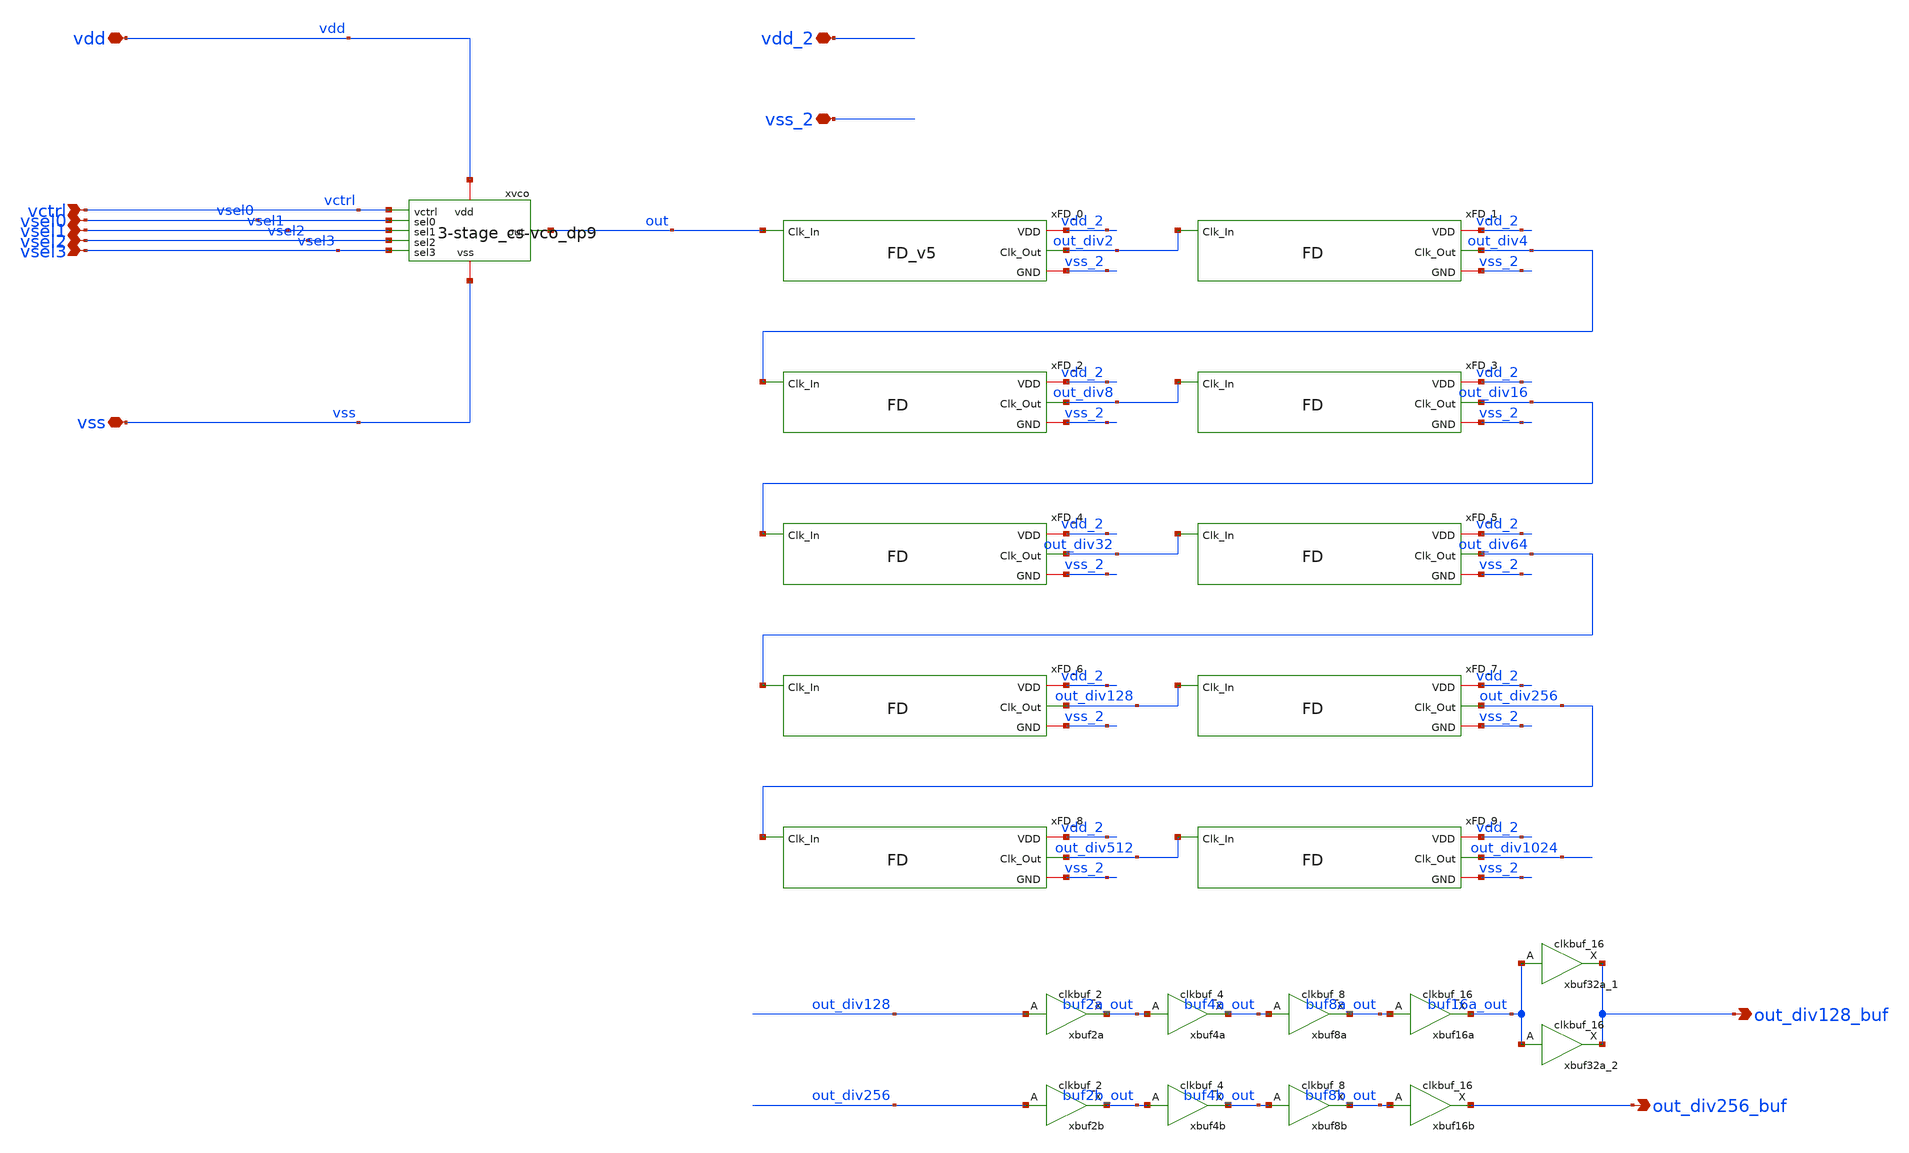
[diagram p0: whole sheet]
** sch_path: xschem/3-stage_cs-vco_dp9/vco_with_fdivs_split_supplies.sch
**.subckt vco_with_fdivs_split_supplies vctrl out_div128_buf vdd vss vsel0 vsel1 vsel2 vsel3
*+ out_div256_buf vdd_2 vss_2
*.ipin vctrl
*.opin out_div128_buf
*.iopin vdd
*.iopin vss
*.ipin vsel0
*.ipin vsel1
*.ipin vsel2
*.ipin vsel3
*.opin out_div256_buf
*.iopin vdd_2
*.iopin vss_2
xvco vdd out vctrl vss vsel0 vsel1 vsel2 vsel3 3-stage_cs-vco_dp9
xFD_0 vdd_2 out_div2 vss_2 out FD_v5
xbuf2a out_div128 vss_2 vss_2 vdd_2 vdd_2 buf2a_out sky130_fd_sc_hd__clkbuf_2
xbuf4a buf2a_out vss_2 vss_2 vdd_2 vdd_2 buf4a_out sky130_fd_sc_hd__clkbuf_4
xbuf8a buf4a_out vss_2 vss_2 vdd_2 vdd_2 buf8a_out sky130_fd_sc_hd__clkbuf_8
xFD_1 vdd_2 out_div4 vss_2 out_div2 FD
xFD_2 vdd_2 out_div8 vss_2 out_div4 FD
xFD_3 vdd_2 out_div16 vss_2 out_div8 FD
xFD_4 vdd_2 out_div32 vss_2 out_div16 FD
xFD_5 vdd_2 out_div64 vss_2 out_div32 FD
xFD_6 vdd_2 out_div128 vss_2 out_div64 FD
xFD_7 vdd_2 out_div256 vss_2 out_div128 FD
xbuf2b out_div256 vss_2 vss_2 vdd_2 vdd_2 buf2b_out sky130_fd_sc_hd__clkbuf_2
xbuf4b buf2b_out vss_2 vss_2 vdd_2 vdd_2 buf4b_out sky130_fd_sc_hd__clkbuf_4
xbuf8b buf4b_out vss_2 vss_2 vdd_2 vdd buf8b_out sky130_fd_sc_hd__clkbuf_8
xFD_8 vdd_2 out_div512 vss_2 out_div256 FD
xFD_9 vdd_2 out_div1024 vss_2 out_div512 FD
xbuf16a buf8a_out vss_2 vss_2 vdd_2 vdd_2 buf16a_out sky130_fd_sc_hd__clkbuf_16
xbuf16b buf8b_out vss_2 vss_2 vdd_2 vdd_2 out_div256_buf sky130_fd_sc_hd__clkbuf_16
xbuf32a_1 buf16a_out vss_2 vss_2 vdd_2 vdd_2 out_div128_buf sky130_fd_sc_hd__clkbuf_16
xbuf32a_2 buf16a_out vss_2 vss_2 vdd_2 vdd_2 out_div128_buf sky130_fd_sc_hd__clkbuf_16
**.ends

* expanding   symbol:  3-stage_cs-vco_dp9.sym # of pins=8
** sym_path: xschem/3-stage_cs-vco_dp9/3-stage_cs-vco_dp9.sym
** sch_path: xschem/3-stage_cs-vco_dp9/3-stage_cs-vco_dp9.sch
.subckt 3-stage_cs-vco_dp9 vdd out vctrl vss sel0 sel1 sel2 sel3
*.iopin vdd
*.iopin vss
*.opin out
*.ipin vctrl
*.ipin sel0
*.ipin sel1
*.ipin sel2
*.ipin sel3
XM25 vgp vgp vdd vdd sky130_fd_pr__pfet_01v8 L=0.18 W=1 nf=1 ad='int((nf+1)/2) * W/nf * 0.29' as='int((nf+2)/2) * W/nf * 0.29'
+ pd='2*int((nf+1)/2) * (W/nf + 0.29)' ps='2*int((nf+2)/2) * (W/nf + 0.29)' nrd='0.29 / W' nrs='0.29 / W'
+ sa=0 sb=0 sd=0 mult=1 m=1
XM26 vgp vctrl vss vss sky130_fd_pr__nfet_01v8 L=0.18 W=1 nf=1 ad='int((nf+1)/2) * W/nf * 0.29' as='int((nf+2)/2) * W/nf * 0.29'
+ pd='2*int((nf+1)/2) * (W/nf + 0.29)' ps='2*int((nf+2)/2) * (W/nf + 0.29)' nrd='0.29 / W' nrs='0.29 / W'
+ sa=0 sb=0 sd=0 mult=1 m=1
XM11C net2 pg2 vdd vdd sky130_fd_pr__pfet_01v8 L=0.18 W=2.4 nf=1 ad='int((nf+1)/2) * W/nf * 0.29' as='int((nf+2)/2) * W/nf * 0.29'
+ pd='2*int((nf+1)/2) * (W/nf + 0.29)' ps='2*int((nf+2)/2) * (W/nf + 0.29)' nrd='0.29 / W' nrs='0.29 / W'
+ sa=0 sb=0 sd=0 mult=1 m=1
XM16A net8 ng0 vss vss sky130_fd_pr__nfet_01v8 L=0.18 W=0.6 nf=1 ad='int((nf+1)/2) * W/nf * 0.29' as='int((nf+2)/2) * W/nf * 0.29'
+ pd='2*int((nf+1)/2) * (W/nf + 0.29)' ps='2*int((nf+2)/2) * (W/nf + 0.29)' nrd='0.29 / W' nrs='0.29 / W'
+ sa=0 sb=0 sd=0 mult=1 m=1
XM1 net3 net5 net2 vdd sky130_fd_pr__pfet_01v8 L=0.15 W=1.4 nf=1 ad='int((nf+1)/2) * W/nf * 0.29' as='int((nf+2)/2) * W/nf * 0.29'
+ pd='2*int((nf+1)/2) * (W/nf + 0.29)' ps='2*int((nf+2)/2) * (W/nf + 0.29)' nrd='0.29 / W' nrs='0.29 / W'
+ sa=0 sb=0 sd=0 mult=1 m=1
XM3 net4 net3 vdd vdd sky130_fd_pr__pfet_01v8 L=0.15 W=0.75 nf=1 ad='int((nf+1)/2) * W/nf * 0.29' as='int((nf+2)/2) * W/nf * 0.29'
+ pd='2*int((nf+1)/2) * (W/nf + 0.29)' ps='2*int((nf+2)/2) * (W/nf + 0.29)' nrd='0.29 / W' nrs='0.29 / W'
+ sa=0 sb=0 sd=0 mult=1 m=1
XM5 net5 net4 vdd vdd sky130_fd_pr__pfet_01v8 L=0.15 W=3 nf=1 ad='int((nf+1)/2) * W/nf * 0.29' as='int((nf+2)/2) * W/nf * 0.29'
+ pd='2*int((nf+1)/2) * (W/nf + 0.29)' ps='2*int((nf+2)/2) * (W/nf + 0.29)' nrd='0.29 / W' nrs='0.29 / W'
+ sa=0 sb=0 sd=0 mult=1 m=1
XM2 net3 net5 net8 vss sky130_fd_pr__nfet_01v8 L=0.15 W=0.72 nf=1 ad='int((nf+1)/2) * W/nf * 0.29' as='int((nf+2)/2) * W/nf * 0.29'
+ pd='2*int((nf+1)/2) * (W/nf + 0.29)' ps='2*int((nf+2)/2) * (W/nf + 0.29)' nrd='0.29 / W' nrs='0.29 / W'
+ sa=0 sb=0 sd=0 mult=1 m=1
XM4 net4 net3 vss vss sky130_fd_pr__nfet_01v8 L=0.15 W=0.5 nf=1 ad='int((nf+1)/2) * W/nf * 0.29' as='int((nf+2)/2) * W/nf * 0.29'
+ pd='2*int((nf+1)/2) * (W/nf + 0.29)' ps='2*int((nf+2)/2) * (W/nf + 0.29)' nrd='0.29 / W' nrs='0.29 / W'
+ sa=0 sb=0 sd=0 mult=1 m=1
XM6 net5 net4 vss vss sky130_fd_pr__nfet_01v8 L=0.15 W=1.44 nf=1 ad='int((nf+1)/2) * W/nf * 0.29' as='int((nf+2)/2) * W/nf * 0.29'
+ pd='2*int((nf+1)/2) * (W/nf + 0.29)' ps='2*int((nf+2)/2) * (W/nf + 0.29)' nrd='0.29 / W' nrs='0.29 / W'
+ sa=0 sb=0 sd=0 mult=1 m=1
XM21 net6 net5 vdd vdd sky130_fd_pr__pfet_01v8 L=0.15 W=0.8 nf=1 ad='int((nf+1)/2) * W/nf * 0.29' as='int((nf+2)/2) * W/nf * 0.29'
+ pd='2*int((nf+1)/2) * (W/nf + 0.29)' ps='2*int((nf+2)/2) * (W/nf + 0.29)' nrd='0.29 / W' nrs='0.29 / W'
+ sa=0 sb=0 sd=0 mult=1 m=1
XM22 net6 net5 vss vss sky130_fd_pr__nfet_01v8 L=0.15 W=0.42 nf=1 ad='int((nf+1)/2) * W/nf * 0.29' as='int((nf+2)/2) * W/nf * 0.29'
+ pd='2*int((nf+1)/2) * (W/nf + 0.29)' ps='2*int((nf+2)/2) * (W/nf + 0.29)' nrd='0.29 / W' nrs='0.29 / W'
+ sa=0 sb=0 sd=0 mult=1 m=1
XM23 out net7 vdd vdd sky130_fd_pr__pfet_01v8 L=0.18 W=6.6 nf=3 ad='int((nf+1)/2) * W/nf * 0.29' as='int((nf+2)/2) * W/nf * 0.29'
+ pd='2*int((nf+1)/2) * (W/nf + 0.29)' ps='2*int((nf+2)/2) * (W/nf + 0.29)' nrd='0.29 / W' nrs='0.29 / W'
+ sa=0 sb=0 sd=0 mult=1 m=1
XM24 out net7 vss vss sky130_fd_pr__nfet_01v8 L=0.18 W=1.29 nf=1 ad='int((nf+1)/2) * W/nf * 0.29' as='int((nf+2)/2) * W/nf * 0.29'
+ pd='2*int((nf+1)/2) * (W/nf + 0.29)' ps='2*int((nf+2)/2) * (W/nf + 0.29)' nrd='0.29 / W' nrs='0.29 / W'
+ sa=0 sb=0 sd=0 mult=1 m=1
XM12 net7 net6 vdd vdd sky130_fd_pr__pfet_01v8 L=0.15 W=2.4 nf=1 ad='int((nf+1)/2) * W/nf * 0.29' as='int((nf+2)/2) * W/nf * 0.29'
+ pd='2*int((nf+1)/2) * (W/nf + 0.29)' ps='2*int((nf+2)/2) * (W/nf + 0.29)' nrd='0.29 / W' nrs='0.29 / W'
+ sa=0 sb=0 sd=0 mult=1 m=1
XM13 net7 net6 vss vss sky130_fd_pr__nfet_01v8 L=0.15 W=1.2 nf=1 ad='int((nf+1)/2) * W/nf * 0.29' as='int((nf+2)/2) * W/nf * 0.29'
+ pd='2*int((nf+1)/2) * (W/nf + 0.29)' ps='2*int((nf+2)/2) * (W/nf + 0.29)' nrd='0.29 / W' nrs='0.29 / W'
+ sa=0 sb=0 sd=0 mult=1 m=1
XMDUM16B vss vss vss vss sky130_fd_pr__nfet_01v8 L=0.18 W=2.4 nf=1 ad='int((nf+1)/2) * W/nf * 0.29' as='int((nf+2)/2) * W/nf * 0.29'
+ pd='2*int((nf+1)/2) * (W/nf + 0.29)' ps='2*int((nf+2)/2) * (W/nf + 0.29)' nrd='0.29 / W' nrs='0.29 / W'
+ sa=0 sb=0 sd=0 mult=1 m=1
XMDUM16 vss vss vss vss sky130_fd_pr__nfet_01v8 L=0.18 W=2.4 nf=1 ad='int((nf+1)/2) * W/nf * 0.29' as='int((nf+2)/2) * W/nf * 0.29'
+ pd='2*int((nf+1)/2) * (W/nf + 0.29)' ps='2*int((nf+2)/2) * (W/nf + 0.29)' nrd='0.29 / W' nrs='0.29 / W'
+ sa=0 sb=0 sd=0 mult=1 m=1
XMDUM26 vss vss vss vss sky130_fd_pr__nfet_01v8 L=0.18 W=1 nf=1 ad='int((nf+1)/2) * W/nf * 0.29' as='int((nf+2)/2) * W/nf * 0.29'
+ pd='2*int((nf+1)/2) * (W/nf + 0.29)' ps='2*int((nf+2)/2) * (W/nf + 0.29)' nrd='0.29 / W' nrs='0.29 / W'
+ sa=0 sb=0 sd=0 mult=1 m=1
XMDUM11B vdd vdd vdd vdd sky130_fd_pr__pfet_01v8 L=0.18 W=2.4 nf=1 ad='int((nf+1)/2) * W/nf * 0.29' as='int((nf+2)/2) * W/nf * 0.29'
+ pd='2*int((nf+1)/2) * (W/nf + 0.29)' ps='2*int((nf+2)/2) * (W/nf + 0.29)' nrd='0.29 / W' nrs='0.29 / W'
+ sa=0 sb=0 sd=0 mult=1 m=1
XMDUM11 vdd vdd vdd vdd sky130_fd_pr__pfet_01v8 L=0.18 W=2.4 nf=1 ad='int((nf+1)/2) * W/nf * 0.29' as='int((nf+2)/2) * W/nf * 0.29'
+ pd='2*int((nf+1)/2) * (W/nf + 0.29)' ps='2*int((nf+2)/2) * (W/nf + 0.29)' nrd='0.29 / W' nrs='0.29 / W'
+ sa=0 sb=0 sd=0 mult=1 m=1
XMDUM25 vdd vdd vdd vdd sky130_fd_pr__pfet_01v8 L=0.18 W=1 nf=1 ad='int((nf+1)/2) * W/nf * 0.29' as='int((nf+2)/2) * W/nf * 0.29'
+ pd='2*int((nf+1)/2) * (W/nf + 0.29)' ps='2*int((nf+2)/2) * (W/nf + 0.29)' nrd='0.29 / W' nrs='0.29 / W'
+ sa=0 sb=0 sd=0 mult=1 m=1
Cnet8 net3 vss 0.87f m=1
Cnet9 net4 vss 1.14f m=1
Cnet10 net5 vss 3.49f m=1
XMDUM26B vss vss vss vss sky130_fd_pr__nfet_01v8 L=0.18 W=1 nf=1 ad='int((nf+1)/2) * W/nf * 0.29' as='int((nf+2)/2) * W/nf * 0.29'
+ pd='2*int((nf+1)/2) * (W/nf + 0.29)' ps='2*int((nf+2)/2) * (W/nf + 0.29)' nrd='0.29 / W' nrs='0.29 / W'
+ sa=0 sb=0 sd=0 mult=1 m=1
XMDUM25B vdd vdd vdd vdd sky130_fd_pr__pfet_01v8 L=0.18 W=1 nf=1 ad='int((nf+1)/2) * W/nf * 0.29' as='int((nf+2)/2) * W/nf * 0.29'
+ pd='2*int((nf+1)/2) * (W/nf + 0.29)' ps='2*int((nf+2)/2) * (W/nf + 0.29)' nrd='0.29 / W' nrs='0.29 / W'
+ sa=0 sb=0 sd=0 mult=1 m=1
x1n vdd ng0 vctrl vss sel0 vco_switch_n
XM16B net8 ng1 vss vss sky130_fd_pr__nfet_01v8 L=0.18 W=1.2 nf=1 ad='int((nf+1)/2) * W/nf * 0.29' as='int((nf+2)/2) * W/nf * 0.29'
+ pd='2*int((nf+1)/2) * (W/nf + 0.29)' ps='2*int((nf+2)/2) * (W/nf + 0.29)' nrd='0.29 / W' nrs='0.29 / W'
+ sa=0 sb=0 sd=0 mult=1 m=1
x2n vdd ng1 vctrl vss sel1 vco_switch_n
XM16C net8 ng2 vss vss sky130_fd_pr__nfet_01v8 L=0.18 W=2.4 nf=1 ad='int((nf+1)/2) * W/nf * 0.29' as='int((nf+2)/2) * W/nf * 0.29'
+ pd='2*int((nf+1)/2) * (W/nf + 0.29)' ps='2*int((nf+2)/2) * (W/nf + 0.29)' nrd='0.29 / W' nrs='0.29 / W'
+ sa=0 sb=0 sd=0 mult=1 m=1
x3n vdd ng2 vctrl vss sel2 vco_switch_n
XM16D net8 ng3 vss vss sky130_fd_pr__nfet_01v8 L=0.18 W=2.4 nf=1 ad='int((nf+1)/2) * W/nf * 0.29' as='int((nf+2)/2) * W/nf * 0.29'
+ pd='2*int((nf+1)/2) * (W/nf + 0.29)' ps='2*int((nf+2)/2) * (W/nf + 0.29)' nrd='0.29 / W' nrs='0.29 / W'
+ sa=0 sb=0 sd=0 mult=2 m=2
x4n vdd ng3 vctrl vss sel3 vco_switch_n
x3p vdd pg2 vgp vss sel2 vco_switch_p
XM11D net2 pg3 vdd vdd sky130_fd_pr__pfet_01v8 L=0.18 W=2.4 nf=1 ad='int((nf+1)/2) * W/nf * 0.29' as='int((nf+2)/2) * W/nf * 0.29'
+ pd='2*int((nf+1)/2) * (W/nf + 0.29)' ps='2*int((nf+2)/2) * (W/nf + 0.29)' nrd='0.29 / W' nrs='0.29 / W'
+ sa=0 sb=0 sd=0 mult=2 m=2
x4p vdd pg3 vgp vss sel3 vco_switch_p
XM11B net2 pg1 vdd vdd sky130_fd_pr__pfet_01v8 L=0.18 W=1.2 nf=1 ad='int((nf+1)/2) * W/nf * 0.29' as='int((nf+2)/2) * W/nf * 0.29'
+ pd='2*int((nf+1)/2) * (W/nf + 0.29)' ps='2*int((nf+2)/2) * (W/nf + 0.29)' nrd='0.29 / W' nrs='0.29 / W'
+ sa=0 sb=0 sd=0 mult=1 m=1
x2p vdd pg1 vgp vss sel1 vco_switch_p
XM11A net2 pg0 vdd vdd sky130_fd_pr__pfet_01v8 L=0.18 W=0.6 nf=1 ad='int((nf+1)/2) * W/nf * 0.29' as='int((nf+2)/2) * W/nf * 0.29'
+ pd='2*int((nf+1)/2) * (W/nf + 0.29)' ps='2*int((nf+2)/2) * (W/nf + 0.29)' nrd='0.29 / W' nrs='0.29 / W'
+ sa=0 sb=0 sd=0 mult=1 m=1
x1p vdd pg0 vgp vss sel0 vco_switch_p
XM16 net8 vctrl vss vss sky130_fd_pr__nfet_01v8 L=0.18 W=0.6 nf=1 ad='int((nf+1)/2) * W/nf * 0.29' as='int((nf+2)/2) * W/nf * 0.29'
+ pd='2*int((nf+1)/2) * (W/nf + 0.29)' ps='2*int((nf+2)/2) * (W/nf + 0.29)' nrd='0.29 / W' nrs='0.29 / W'
+ sa=0 sb=0 sd=0 mult=1 m=1
XM11 net2 vgp vdd vdd sky130_fd_pr__pfet_01v8 L=0.18 W=0.6 nf=1 ad='int((nf+1)/2) * W/nf * 0.29' as='int((nf+2)/2) * W/nf * 0.29'
+ pd='2*int((nf+1)/2) * (W/nf + 0.29)' ps='2*int((nf+2)/2) * (W/nf + 0.29)' nrd='0.29 / W' nrs='0.29 / W'
+ sa=0 sb=0 sd=0 mult=1 m=1
.ends


* expanding   symbol:  FD_v5.sym # of pins=4
** sym_path: xschem/3-stage_cs-vco_dp9/FD_v5.sym
** sch_path: xschem/3-stage_cs-vco_dp9/FD_v5.sch
.subckt FD_v5 VDD Clk_Out GND Clk_In
*.ipin Clk_In
*.iopin VDD
*.iopin GND
*.opin Clk_Out
XMPbuf1 7 6 VDD VDD sky130_fd_pr__pfet_01v8 L=0.15 W=1.44 nf=1 ad='int((nf+1)/2) * W/nf * 0.29' as='int((nf+2)/2) * W/nf * 0.29'
+ pd='2*int((nf+1)/2) * (W/nf + 0.29)' ps='2*int((nf+2)/2) * (W/nf + 0.29)' nrd='0.29 / W' nrs='0.29 / W'
+ sa=0 sb=0 sd=0 mult=1 m=1
XMNbuf1 7 6 GND GND sky130_fd_pr__nfet_01v8 L=0.15 W=0.84 nf=1 ad='int((nf+1)/2) * W/nf * 0.29' as='int((nf+2)/2) * W/nf * 0.29'
+ pd='2*int((nf+1)/2) * (W/nf + 0.29)' ps='2*int((nf+2)/2) * (W/nf + 0.29)' nrd='0.29 / W' nrs='0.29 / W'
+ sa=0 sb=0 sd=0 mult=1 m=1
XMPClkin Clk_In_buf Clkb_buf VDD VDD sky130_fd_pr__pfet_01v8 L=0.15 W=1.44 nf=1 ad='int((nf+1)/2) * W/nf * 0.29'
+ as='int((nf+2)/2) * W/nf * 0.29' pd='2*int((nf+1)/2) * (W/nf + 0.29)' ps='2*int((nf+2)/2) * (W/nf + 0.29)'
+ nrd='0.29 / W' nrs='0.29 / W' sa=0 sb=0 sd=0 mult=4 m=4
XMNClkin Clk_In_buf Clkb_buf GND GND sky130_fd_pr__nfet_01v8 L=0.15 W=0.84 nf=1 ad='int((nf+1)/2) * W/nf * 0.29'
+ as='int((nf+2)/2) * W/nf * 0.29' pd='2*int((nf+1)/2) * (W/nf + 0.29)' ps='2*int((nf+2)/2) * (W/nf + 0.29)'
+ nrd='0.29 / W' nrs='0.29 / W' sa=0 sb=0 sd=0 mult=3 m=3
XMPinv2 5 4 VDD VDD sky130_fd_pr__pfet_01v8 L=0.15 W=1.44 nf=1 ad='int((nf+1)/2) * W/nf * 0.29' as='int((nf+2)/2) * W/nf * 0.29'
+ pd='2*int((nf+1)/2) * (W/nf + 0.29)' ps='2*int((nf+2)/2) * (W/nf + 0.29)' nrd='0.29 / W' nrs='0.29 / W'
+ sa=0 sb=0 sd=0 mult=4 m=4
XMNinv2 5 4 GND GND sky130_fd_pr__nfet_01v8 L=0.15 W=0.84 nf=1 ad='int((nf+1)/2) * W/nf * 0.29' as='int((nf+2)/2) * W/nf * 0.29'
+ pd='2*int((nf+1)/2) * (W/nf + 0.29)' ps='2*int((nf+2)/2) * (W/nf + 0.29)' nrd='0.29 / W' nrs='0.29 / W'
+ sa=0 sb=0 sd=0 mult=3 m=3
XMPinv1 3 2 VDD VDD sky130_fd_pr__pfet_01v8 L=0.15 W=1.44 nf=1 ad='int((nf+1)/2) * W/nf * 0.29' as='int((nf+2)/2) * W/nf * 0.29'
+ pd='2*int((nf+1)/2) * (W/nf + 0.29)' ps='2*int((nf+2)/2) * (W/nf + 0.29)' nrd='0.29 / W' nrs='0.29 / W'
+ sa=0 sb=0 sd=0 mult=4 m=4
XMNinv1 3 2 GND GND sky130_fd_pr__nfet_01v8 L=0.15 W=0.84 nf=1 ad='int((nf+1)/2) * W/nf * 0.29' as='int((nf+2)/2) * W/nf * 0.29'
+ pd='2*int((nf+1)/2) * (W/nf + 0.29)' ps='2*int((nf+2)/2) * (W/nf + 0.29)' nrd='0.29 / W' nrs='0.29 / W'
+ sa=0 sb=0 sd=0 mult=3 m=3
XMPTgate1 4 Clkb_buf 3 VDD sky130_fd_pr__pfet_01v8 L=0.15 W=1.44 nf=1 ad='int((nf+1)/2) * W/nf * 0.29'
+ as='int((nf+2)/2) * W/nf * 0.29' pd='2*int((nf+1)/2) * (W/nf + 0.29)' ps='2*int((nf+2)/2) * (W/nf + 0.29)'
+ nrd='0.29 / W' nrs='0.29 / W' sa=0 sb=0 sd=0 mult=5 m=5
XMNTgate1 4 Clk_In_buf 3 GND sky130_fd_pr__nfet_01v8 L=0.15 W=0.84 nf=1 ad='int((nf+1)/2) * W/nf * 0.29'
+ as='int((nf+2)/2) * W/nf * 0.29' pd='2*int((nf+1)/2) * (W/nf + 0.29)' ps='2*int((nf+2)/2) * (W/nf + 0.29)'
+ nrd='0.29 / W' nrs='0.29 / W' sa=0 sb=0 sd=0 mult=8 m=8
XMPTgate2 6 Clk_In_buf 5 VDD sky130_fd_pr__pfet_01v8 L=0.15 W=1.44 nf=1 ad='int((nf+1)/2) * W/nf * 0.29'
+ as='int((nf+2)/2) * W/nf * 0.29' pd='2*int((nf+1)/2) * (W/nf + 0.29)' ps='2*int((nf+2)/2) * (W/nf + 0.29)'
+ nrd='0.29 / W' nrs='0.29 / W' sa=0 sb=0 sd=0 mult=5 m=5
XMNTgate2 6 Clkb_buf 5 GND sky130_fd_pr__nfet_01v8 L=0.15 W=0.84 nf=1 ad='int((nf+1)/2) * W/nf * 0.29'
+ as='int((nf+2)/2) * W/nf * 0.29' pd='2*int((nf+1)/2) * (W/nf + 0.29)' ps='2*int((nf+2)/2) * (W/nf + 0.29)'
+ nrd='0.29 / W' nrs='0.29 / W' sa=0 sb=0 sd=0 mult=8 m=8
XMPbuf2 Clk_Out 7 VDD VDD sky130_fd_pr__pfet_01v8 L=0.15 W=1.44 nf=1 ad='int((nf+1)/2) * W/nf * 0.29'
+ as='int((nf+2)/2) * W/nf * 0.29' pd='2*int((nf+1)/2) * (W/nf + 0.29)' ps='2*int((nf+2)/2) * (W/nf + 0.29)'
+ nrd='0.29 / W' nrs='0.29 / W' sa=0 sb=0 sd=0 mult=2 m=2
XMNbuf2 Clk_Out 7 GND GND sky130_fd_pr__nfet_01v8 L=0.15 W=0.84 nf=1 ad='int((nf+1)/2) * W/nf * 0.29'
+ as='int((nf+2)/2) * W/nf * 0.29' pd='2*int((nf+1)/2) * (W/nf + 0.29)' ps='2*int((nf+2)/2) * (W/nf + 0.29)'
+ nrd='0.29 / W' nrs='0.29 / W' sa=0 sb=0 sd=0 mult=2 m=2
XMPfb 2 6 VDD VDD sky130_fd_pr__pfet_01v8 L=0.15 W=1.44 nf=1 ad='int((nf+1)/2) * W/nf * 0.29' as='int((nf+2)/2) * W/nf * 0.29'
+ pd='2*int((nf+1)/2) * (W/nf + 0.29)' ps='2*int((nf+2)/2) * (W/nf + 0.29)' nrd='0.29 / W' nrs='0.29 / W'
+ sa=0 sb=0 sd=0 mult=4 m=4
XMNfb 2 6 GND GND sky130_fd_pr__nfet_01v8 L=0.15 W=0.84 nf=1 ad='int((nf+1)/2) * W/nf * 0.29' as='int((nf+2)/2) * W/nf * 0.29'
+ pd='2*int((nf+1)/2) * (W/nf + 0.29)' ps='2*int((nf+2)/2) * (W/nf + 0.29)' nrd='0.29 / W' nrs='0.29 / W'
+ sa=0 sb=0 sd=0 mult=3 m=3
XMPClkin_b2 net1 Clkb_int VDD VDD sky130_fd_pr__pfet_01v8 L=0.15 W=1.44 nf=1 ad='int((nf+1)/2) * W/nf * 0.29'
+ as='int((nf+2)/2) * W/nf * 0.29' pd='2*int((nf+1)/2) * (W/nf + 0.29)' ps='2*int((nf+2)/2) * (W/nf + 0.29)'
+ nrd='0.29 / W' nrs='0.29 / W' sa=0 sb=0 sd=0 mult=5 m=5
XMNClkin_b2 net1 Clkb_int GND GND sky130_fd_pr__nfet_01v8 L=0.15 W=0.84 nf=1 ad='int((nf+1)/2) * W/nf * 0.29'
+ as='int((nf+2)/2) * W/nf * 0.29' pd='2*int((nf+1)/2) * (W/nf + 0.29)' ps='2*int((nf+2)/2) * (W/nf + 0.29)'
+ nrd='0.29 / W' nrs='0.29 / W' sa=0 sb=0 sd=0 mult=3 m=3
XMPClkin_b1 Clkb_int Clk_In VDD VDD sky130_fd_pr__pfet_01v8 L=0.15 W=1.44 nf=1 ad='int((nf+1)/2) * W/nf * 0.29'
+ as='int((nf+2)/2) * W/nf * 0.29' pd='2*int((nf+1)/2) * (W/nf + 0.29)' ps='2*int((nf+2)/2) * (W/nf + 0.29)'
+ nrd='0.29 / W' nrs='0.29 / W' sa=0 sb=0 sd=0 mult=2 m=2
XMNClkin_b1 Clkb_int Clk_In GND GND sky130_fd_pr__nfet_01v8 L=0.15 W=0.84 nf=1 ad='int((nf+1)/2) * W/nf * 0.29'
+ as='int((nf+2)/2) * W/nf * 0.29' pd='2*int((nf+1)/2) * (W/nf + 0.29)' ps='2*int((nf+2)/2) * (W/nf + 0.29)'
+ nrd='0.29 / W' nrs='0.29 / W' sa=0 sb=0 sd=0 mult=2 m=2
XMPClkin_b3 Clkb_buf net1 VDD VDD sky130_fd_pr__pfet_01v8 L=0.15 W=1.44 nf=1 ad='int((nf+1)/2) * W/nf * 0.29'
+ as='int((nf+2)/2) * W/nf * 0.29' pd='2*int((nf+1)/2) * (W/nf + 0.29)' ps='2*int((nf+2)/2) * (W/nf + 0.29)'
+ nrd='0.29 / W' nrs='0.29 / W' sa=0 sb=0 sd=0 mult=7 m=7
XMNClkin_b3 Clkb_buf net1 GND GND sky130_fd_pr__nfet_01v8 L=0.15 W=0.84 nf=1 ad='int((nf+1)/2) * W/nf * 0.29'
+ as='int((nf+2)/2) * W/nf * 0.29' pd='2*int((nf+1)/2) * (W/nf + 0.29)' ps='2*int((nf+2)/2) * (W/nf + 0.29)'
+ nrd='0.29 / W' nrs='0.29 / W' sa=0 sb=0 sd=0 mult=5 m=5
.ends


* expanding   symbol:  FD.sym # of pins=4
** sym_path: xschem/3-stage_cs-vco_dp9/FD.sym
** sch_path: xschem/3-stage_cs-vco_dp9/FD.sch
.subckt FD VDD Clk_Out GND Clk_In
*.ipin Clk_In
*.iopin VDD
*.iopin GND
*.opin Clk_Out
XM15 7 6 VDD VDD sky130_fd_pr__pfet_01v8 L=0.15 W=0.72 nf=1 ad='int((nf+1)/2) * W/nf * 0.29' as='int((nf+2)/2) * W/nf * 0.29'
+ pd='2*int((nf+1)/2) * (W/nf + 0.29)' ps='2*int((nf+2)/2) * (W/nf + 0.29)' nrd='0.29 / W' nrs='0.29 / W'
+ sa=0 sb=0 sd=0 mult=1 m=1
XM16 7 6 GND GND sky130_fd_pr__nfet_01v8 L=0.15 W=0.42 nf=1 ad='int((nf+1)/2) * W/nf * 0.29' as='int((nf+2)/2) * W/nf * 0.29'
+ pd='2*int((nf+1)/2) * (W/nf + 0.29)' ps='2*int((nf+2)/2) * (W/nf + 0.29)' nrd='0.29 / W' nrs='0.29 / W'
+ sa=0 sb=0 sd=0 mult=1 m=1
XM11 2 6 VDD VDD sky130_fd_pr__pfet_01v8 L=0.15 W=0.72 nf=1 ad='int((nf+1)/2) * W/nf * 0.29' as='int((nf+2)/2) * W/nf * 0.29'
+ pd='2*int((nf+1)/2) * (W/nf + 0.29)' ps='2*int((nf+2)/2) * (W/nf + 0.29)' nrd='0.29 / W' nrs='0.29 / W'
+ sa=0 sb=0 sd=0 mult=1 m=1
XM12 2 6 GND GND sky130_fd_pr__nfet_01v8 L=0.15 W=0.42 nf=1 ad='int((nf+1)/2) * W/nf * 0.29' as='int((nf+2)/2) * W/nf * 0.29'
+ pd='2*int((nf+1)/2) * (W/nf + 0.29)' ps='2*int((nf+2)/2) * (W/nf + 0.29)' nrd='0.29 / W' nrs='0.29 / W'
+ sa=0 sb=0 sd=0 mult=1 m=1
XM13 Clkb Clk_In VDD VDD sky130_fd_pr__pfet_01v8 L=0.15 W=0.72 nf=1 ad='int((nf+1)/2) * W/nf * 0.29'
+ as='int((nf+2)/2) * W/nf * 0.29' pd='2*int((nf+1)/2) * (W/nf + 0.29)' ps='2*int((nf+2)/2) * (W/nf + 0.29)'
+ nrd='0.29 / W' nrs='0.29 / W' sa=0 sb=0 sd=0 mult=1 m=1
XM14 Clkb Clk_In GND GND sky130_fd_pr__nfet_01v8 L=0.15 W=0.42 nf=1 ad='int((nf+1)/2) * W/nf * 0.29'
+ as='int((nf+2)/2) * W/nf * 0.29' pd='2*int((nf+1)/2) * (W/nf + 0.29)' ps='2*int((nf+2)/2) * (W/nf + 0.29)'
+ nrd='0.29 / W' nrs='0.29 / W' sa=0 sb=0 sd=0 mult=1 m=1
XM7 5 4 VDD VDD sky130_fd_pr__pfet_01v8 L=0.15 W=0.72 nf=1 ad='int((nf+1)/2) * W/nf * 0.29' as='int((nf+2)/2) * W/nf * 0.29'
+ pd='2*int((nf+1)/2) * (W/nf + 0.29)' ps='2*int((nf+2)/2) * (W/nf + 0.29)' nrd='0.29 / W' nrs='0.29 / W'
+ sa=0 sb=0 sd=0 mult=1 m=1
XM8 5 4 GND GND sky130_fd_pr__nfet_01v8 L=0.15 W=0.42 nf=1 ad='int((nf+1)/2) * W/nf * 0.29' as='int((nf+2)/2) * W/nf * 0.29'
+ pd='2*int((nf+1)/2) * (W/nf + 0.29)' ps='2*int((nf+2)/2) * (W/nf + 0.29)' nrd='0.29 / W' nrs='0.29 / W'
+ sa=0 sb=0 sd=0 mult=1 m=1
XM1 3 2 VDD VDD sky130_fd_pr__pfet_01v8 L=0.15 W=0.72 nf=1 ad='int((nf+1)/2) * W/nf * 0.29' as='int((nf+2)/2) * W/nf * 0.29'
+ pd='2*int((nf+1)/2) * (W/nf + 0.29)' ps='2*int((nf+2)/2) * (W/nf + 0.29)' nrd='0.29 / W' nrs='0.29 / W'
+ sa=0 sb=0 sd=0 mult=1 m=1
XM2 3 2 GND GND sky130_fd_pr__nfet_01v8 L=0.15 W=0.42 nf=1 ad='int((nf+1)/2) * W/nf * 0.29' as='int((nf+2)/2) * W/nf * 0.29'
+ pd='2*int((nf+1)/2) * (W/nf + 0.29)' ps='2*int((nf+2)/2) * (W/nf + 0.29)' nrd='0.29 / W' nrs='0.29 / W'
+ sa=0 sb=0 sd=0 mult=1 m=1
XM3 4 Clkb 3 VDD sky130_fd_pr__pfet_01v8 L=0.15 W=0.42 nf=1 ad='int((nf+1)/2) * W/nf * 0.29' as='int((nf+2)/2) * W/nf * 0.29'
+ pd='2*int((nf+1)/2) * (W/nf + 0.29)' ps='2*int((nf+2)/2) * (W/nf + 0.29)' nrd='0.29 / W' nrs='0.29 / W'
+ sa=0 sb=0 sd=0 mult=1 m=1
XM4 4 Clk_In 3 GND sky130_fd_pr__nfet_01v8 L=0.15 W=0.84 nf=1 ad='int((nf+1)/2) * W/nf * 0.29' as='int((nf+2)/2) * W/nf * 0.29'
+ pd='2*int((nf+1)/2) * (W/nf + 0.29)' ps='2*int((nf+2)/2) * (W/nf + 0.29)' nrd='0.29 / W' nrs='0.29 / W'
+ sa=0 sb=0 sd=0 mult=1 m=1
XM9 6 Clk_In 5 VDD sky130_fd_pr__pfet_01v8 L=0.15 W=0.42 nf=1 ad='int((nf+1)/2) * W/nf * 0.29' as='int((nf+2)/2) * W/nf * 0.29'
+ pd='2*int((nf+1)/2) * (W/nf + 0.29)' ps='2*int((nf+2)/2) * (W/nf + 0.29)' nrd='0.29 / W' nrs='0.29 / W'
+ sa=0 sb=0 sd=0 mult=1 m=1
XM10 6 Clkb 5 GND sky130_fd_pr__nfet_01v8 L=0.15 W=0.84 nf=1 ad='int((nf+1)/2) * W/nf * 0.29' as='int((nf+2)/2) * W/nf * 0.29'
+ pd='2*int((nf+1)/2) * (W/nf + 0.29)' ps='2*int((nf+2)/2) * (W/nf + 0.29)' nrd='0.29 / W' nrs='0.29 / W'
+ sa=0 sb=0 sd=0 mult=1 m=1
XM19 Clk_Out 7 VDD VDD sky130_fd_pr__pfet_01v8 L=0.15 W=0.72 nf=1 ad='int((nf+1)/2) * W/nf * 0.29' as='int((nf+2)/2) * W/nf * 0.29'
+ pd='2*int((nf+1)/2) * (W/nf + 0.29)' ps='2*int((nf+2)/2) * (W/nf + 0.29)' nrd='0.29 / W' nrs='0.29 / W'
+ sa=0 sb=0 sd=0 mult=1 m=1
XM20 Clk_Out 7 GND GND sky130_fd_pr__nfet_01v8 L=0.15 W=0.42 nf=1 ad='int((nf+1)/2) * W/nf * 0.29' as='int((nf+2)/2) * W/nf * 0.29'
+ pd='2*int((nf+1)/2) * (W/nf + 0.29)' ps='2*int((nf+2)/2) * (W/nf + 0.29)' nrd='0.29 / W' nrs='0.29 / W'
+ sa=0 sb=0 sd=0 mult=1 m=1
.ends


* expanding   symbol:  vco_switch_n.sym # of pins=5
** sym_path: xschem/3-stage_cs-vco_dp9/vco_switch_n.sym
** sch_path: xschem/3-stage_cs-vco_dp9/vco_switch_n.sch
.subckt vco_switch_n vdd out in vss sel
*.ipin in
*.ipin sel
*.opin out
*.iopin vss
*.iopin vdd
XM26 in sel out vss sky130_fd_pr__nfet_01v8 L=0.18 W=0.42 nf=1 ad='int((nf+1)/2) * W/nf * 0.29' as='int((nf+2)/2) * W/nf * 0.29'
+ pd='2*int((nf+1)/2) * (W/nf + 0.29)' ps='2*int((nf+2)/2) * (W/nf + 0.29)' nrd='0.29 / W' nrs='0.29 / W'
+ sa=0 sb=0 sd=0 mult=1 m=1
XM25 out selb in vdd sky130_fd_pr__pfet_01v8 L=0.18 W=0.72 nf=1 ad='int((nf+1)/2) * W/nf * 0.29' as='int((nf+2)/2) * W/nf * 0.29'
+ pd='2*int((nf+1)/2) * (W/nf + 0.29)' ps='2*int((nf+2)/2) * (W/nf + 0.29)' nrd='0.29 / W' nrs='0.29 / W'
+ sa=0 sb=0 sd=0 mult=1 m=1
XM1 out selb vss vss sky130_fd_pr__nfet_01v8 L=0.18 W=0.42 nf=1 ad='int((nf+1)/2) * W/nf * 0.29' as='int((nf+2)/2) * W/nf * 0.29'
+ pd='2*int((nf+1)/2) * (W/nf + 0.29)' ps='2*int((nf+2)/2) * (W/nf + 0.29)' nrd='0.29 / W' nrs='0.29 / W'
+ sa=0 sb=0 sd=0 mult=1 m=1
x1 sel vss vss vdd vdd selb sky130_fd_sc_hd__inv_1
**** begin user architecture code

.include /usr/local/share/pdk/sky130A/libs.ref/sky130_fd_sc_hd/spice/sky130_fd_sc_hd.spice

**** end user architecture code
.ends


* expanding   symbol:  vco_switch_p.sym # of pins=5
** sym_path: xschem/3-stage_cs-vco_dp9/vco_switch_p.sym
** sch_path: xschem/3-stage_cs-vco_dp9/vco_switch_p.sch
.subckt vco_switch_p vdd out in vss sel
*.ipin in
*.ipin sel
*.opin out
*.iopin vss
*.iopin vdd
XM26 in sel out vss sky130_fd_pr__nfet_01v8 L=0.18 W=0.42 nf=1 ad='int((nf+1)/2) * W/nf * 0.29' as='int((nf+2)/2) * W/nf * 0.29'
+ pd='2*int((nf+1)/2) * (W/nf + 0.29)' ps='2*int((nf+2)/2) * (W/nf + 0.29)' nrd='0.29 / W' nrs='0.29 / W'
+ sa=0 sb=0 sd=0 mult=1 m=1
XM25 out selb in vdd sky130_fd_pr__pfet_01v8 L=0.18 W=0.72 nf=1 ad='int((nf+1)/2) * W/nf * 0.29' as='int((nf+2)/2) * W/nf * 0.29'
+ pd='2*int((nf+1)/2) * (W/nf + 0.29)' ps='2*int((nf+2)/2) * (W/nf + 0.29)' nrd='0.29 / W' nrs='0.29 / W'
+ sa=0 sb=0 sd=0 mult=1 m=1
x1 sel vss vss vdd vdd selb sky130_fd_sc_hd__inv_1
XM1 vdd sel out vdd sky130_fd_pr__pfet_01v8 L=0.18 W=0.72 nf=1 ad='int((nf+1)/2) * W/nf * 0.29' as='int((nf+2)/2) * W/nf * 0.29'
+ pd='2*int((nf+1)/2) * (W/nf + 0.29)' ps='2*int((nf+2)/2) * (W/nf + 0.29)' nrd='0.29 / W' nrs='0.29 / W'
+ sa=0 sb=0 sd=0 mult=1 m=1
**** begin user architecture code

.include /usr/local/share/pdk/sky130A/libs.ref/sky130_fd_sc_hd/spice/sky130_fd_sc_hd.spice

**** end user architecture code
.ends

.end
